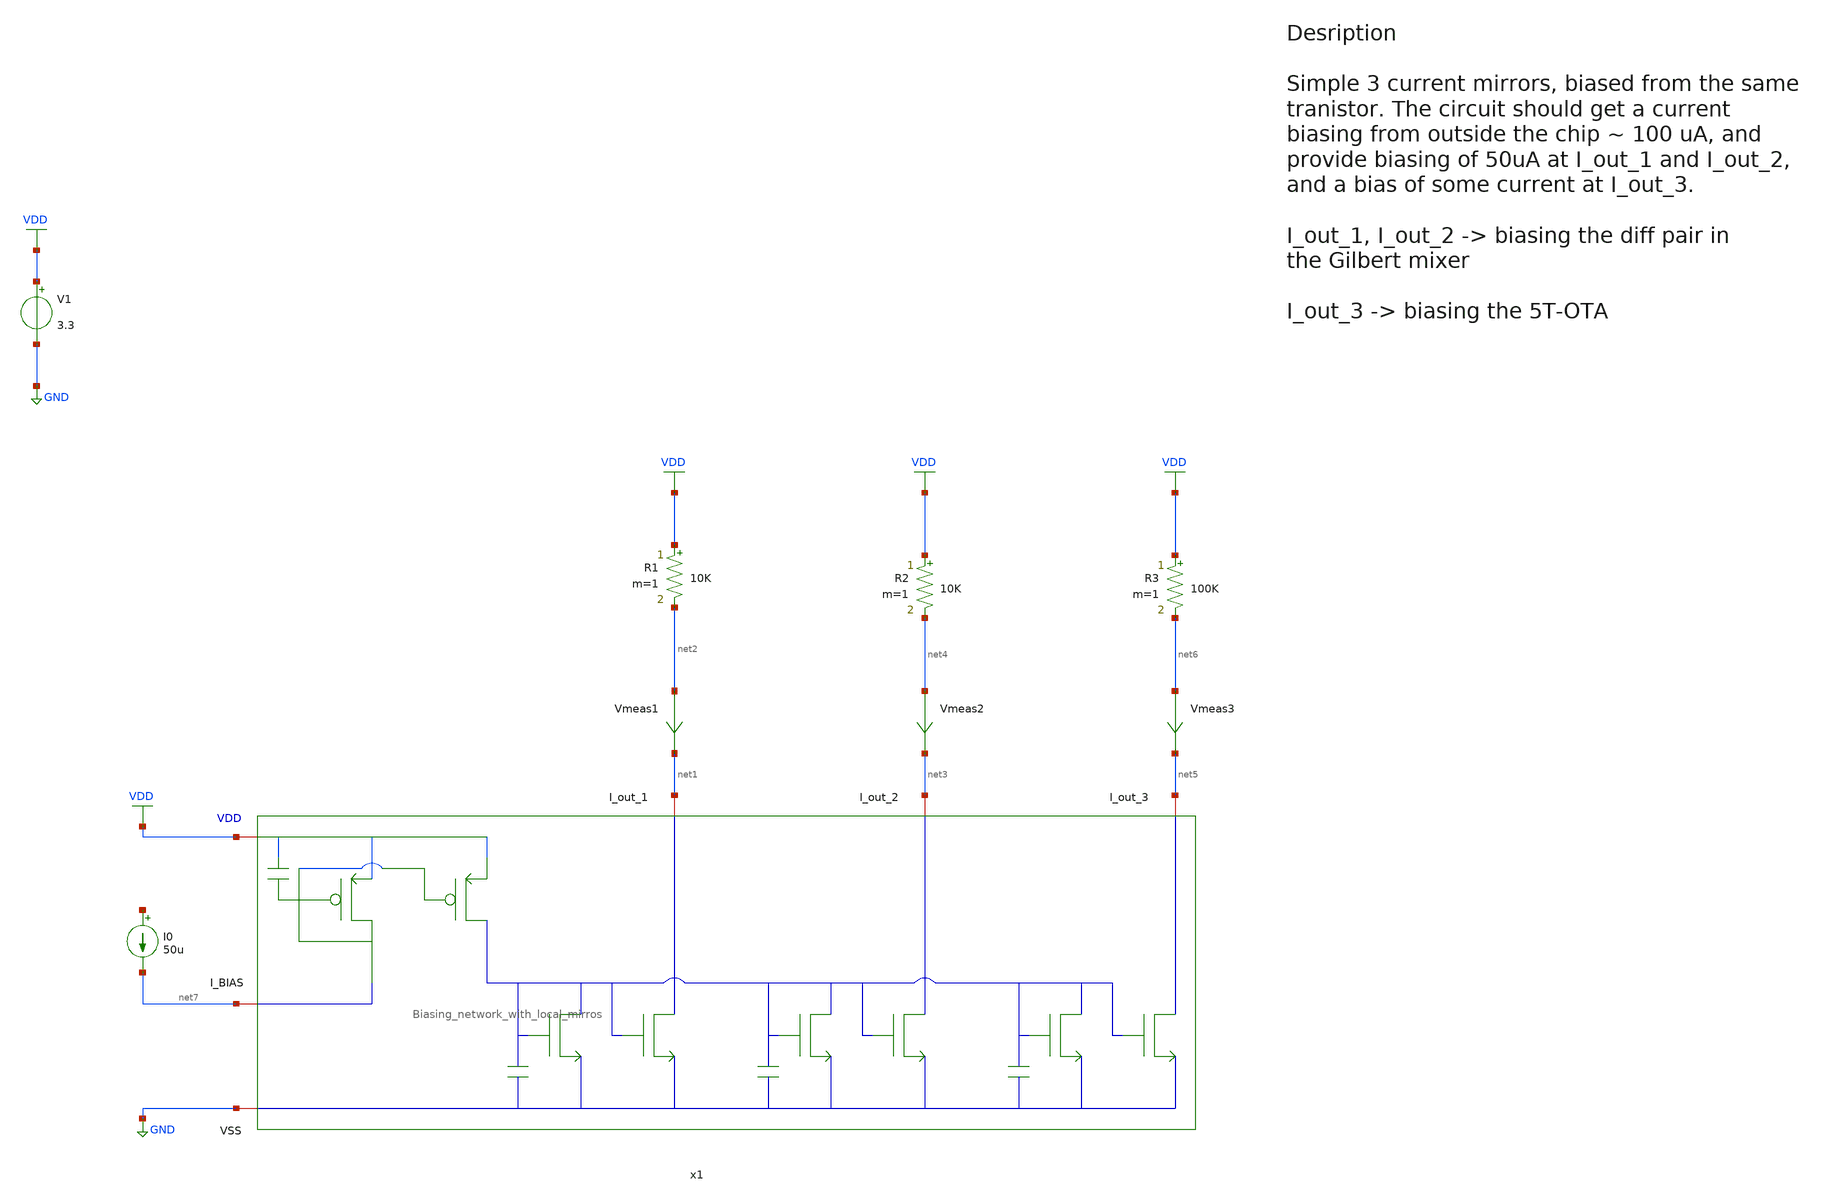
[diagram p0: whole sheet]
** sch_path: src/design_tb/Local_mirror_biasing_tb.sch
**.subckt Local_mirror_biasing_tb
I0 net8 net7 50u
V1 VDD GND 3.3
Vmeas1 net2 net1 0
.save i(vmeas1)
Vmeas2 net4 net3 0
.save i(vmeas2)
Vmeas3 net6 net5 0
.save i(vmeas3)
R1 VDD net2 10K m=1
R2 VDD net4 10K m=1
R3 VDD net6 100K m=1
x1 VDD net1 net3 net5 net7 GND Biasing_network_with_local_mirros
**** begin user architecture code

.include $::180MCU_MODELS/design.ngspice
.lib $::180MCU_MODELS/sm141064.ngspice typical
.lib $::180MCU_MODELS/sm141064.ngspice mimcap_typical
.lib $::180MCU_MODELS/sm141064.ngspice cap_mim
.lib $::180MCU_MODELS/sm141064.ngspice res_typical
.lib $::180MCU_MODELS/sm141064.ngspice diode_typical
.lib $::180MCU_MODELS/sm141064.ngspice bjt_typical
.lib $::180MCU_MODELS/sm141064.ngspice moscap_typical
.lib $::180MCU_MODELS/sm141064.ngspice mimcap_typical



* let sets vectors to a plot, while set sets a variable, globally accessible in .control
.control

    * operating point
    op
    show

    write Local_mirror_biasing_tb.raw

    set appendwrite

    * Transient analysis to observe mixing operation
    tran 2p 0.01u
    write Local_mirror_biasing_tb.raw

.endc


**** end user architecture code
**.ends
.GLOBAL GND
.GLOBAL VDD
.end
